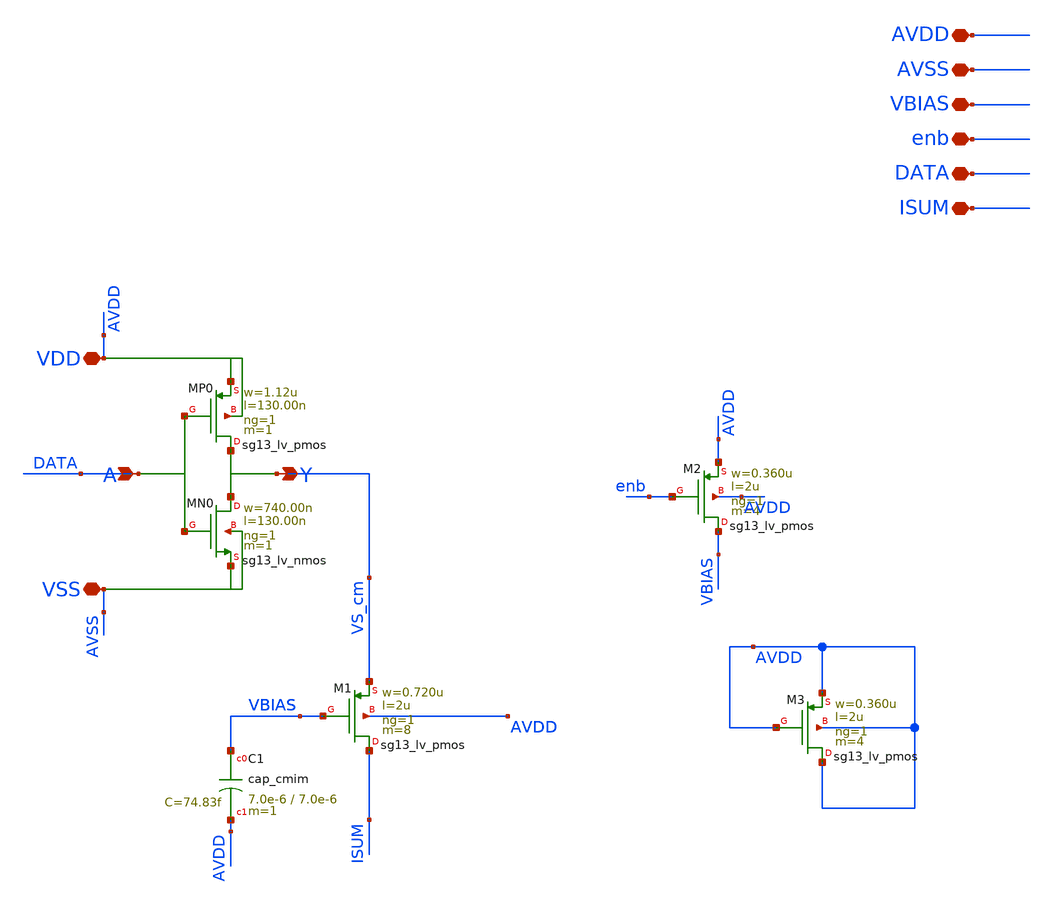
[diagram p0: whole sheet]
** sch_path: current_generator/analog/DAC/dac_bin_2.sch
* IHP-GmbH/IHP-Open-PDK/ihp-sg13cmos5l/libs.tech/xschem/sg13cmos5l_stdcells/sg13g2_inv_1.sch:
* Copyright 2025 IHP PDK Authors
* Licensed under the Apache License, Version 2.0 (the "License");
**.subckt dac_bin_2 AVDD AVSS VBIAS enb DATA ISUM
*.iopin AVDD
*.iopin AVSS
*.iopin VBIAS
*.iopin enb
*.iopin DATA
*.iopin ISUM
XM1 ISUM VBIAS VS_cm AVDD sg13_lv_pmos w=0.720u l=2u ng=1 m=8 mm_ok=1
x1 VS_cm DATA AVDD AVSS sg13g2_inv_1
XC1 VBIAS AVDD cap_cmim w=7.0e-6 l=7.0e-6 m=1 mm_ok=1
XM2 VBIAS enb AVDD AVDD sg13_lv_pmos w=0.360u l=2u ng=1 m=4 mm_ok=1
XM3 AVDD AVDD AVDD AVDD sg13_lv_pmos w=0.360u l=2u ng=1 m=4 mm_ok=1
**.ends

* expanding   symbol:  sg13g2_stdcells/sg13g2_inv_1.sch # of pins=4
** sym_path: sg13g2_stdcells/sg13g2_inv_1.sch
** sch_path: sg13g2_stdcells/sg13g2_inv_1.sch
.subckt sg13g2_inv_1 Y A VDD VSS
*.opin Y
*.ipin A
*.iopin VDD
*.iopin VSS
XMN0 Y A VSS VSS sg13_lv_nmos w=740.00n l=130.00n ng=1 m=1 mm_ok=1
XMP0 Y A VDD VDD sg13_lv_pmos w=1.12u l=130.00n ng=1 m=1 mm_ok=1
.ends

.end
